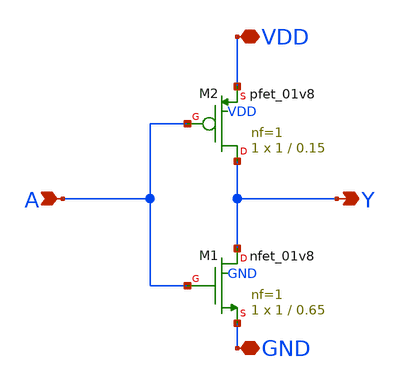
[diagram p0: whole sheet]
** sch_path: sar-adc/inv.sch
**.subckt inv GND VDD A Y
*.iopin GND
*.iopin VDD
*.ipin A
*.opin Y
XM1 Y A GND GND sky130_fd_pr__nfet_01v8 L=0.65 W=1 nf=1 ad='int((1 + 1)/2) * 1 / 1 * 0.29' as='int((1 + 2)/2) * 1 / 1 * 0.29'
+ pd='2*int((1 + 1)/2) * (1 / 1 + 0.29)' ps='2*int((1 + 2)/2) * (1 / 1 + 0.29)' nrd='0.29 / 1 ' nrs='0.29 / 1 '
+ sa=0 sb=0 sd=0 mult=1 m=1
XM2 Y A VDD VDD sky130_fd_pr__pfet_01v8 L=0.15 W=1 nf=1 ad='int((1 + 1)/2) * 1 / 1 * 0.29' as='int((1 + 2)/2) * 1 / 1 * 0.29'
+ pd='2*int((1 + 1)/2) * (1 / 1 + 0.29)' ps='2*int((1 + 2)/2) * (1 / 1 + 0.29)' nrd='0.29 / 1 ' nrs='0.29 / 1 '
+ sa=0 sb=0 sd=0 mult=1 m=1
**.ends
.end
